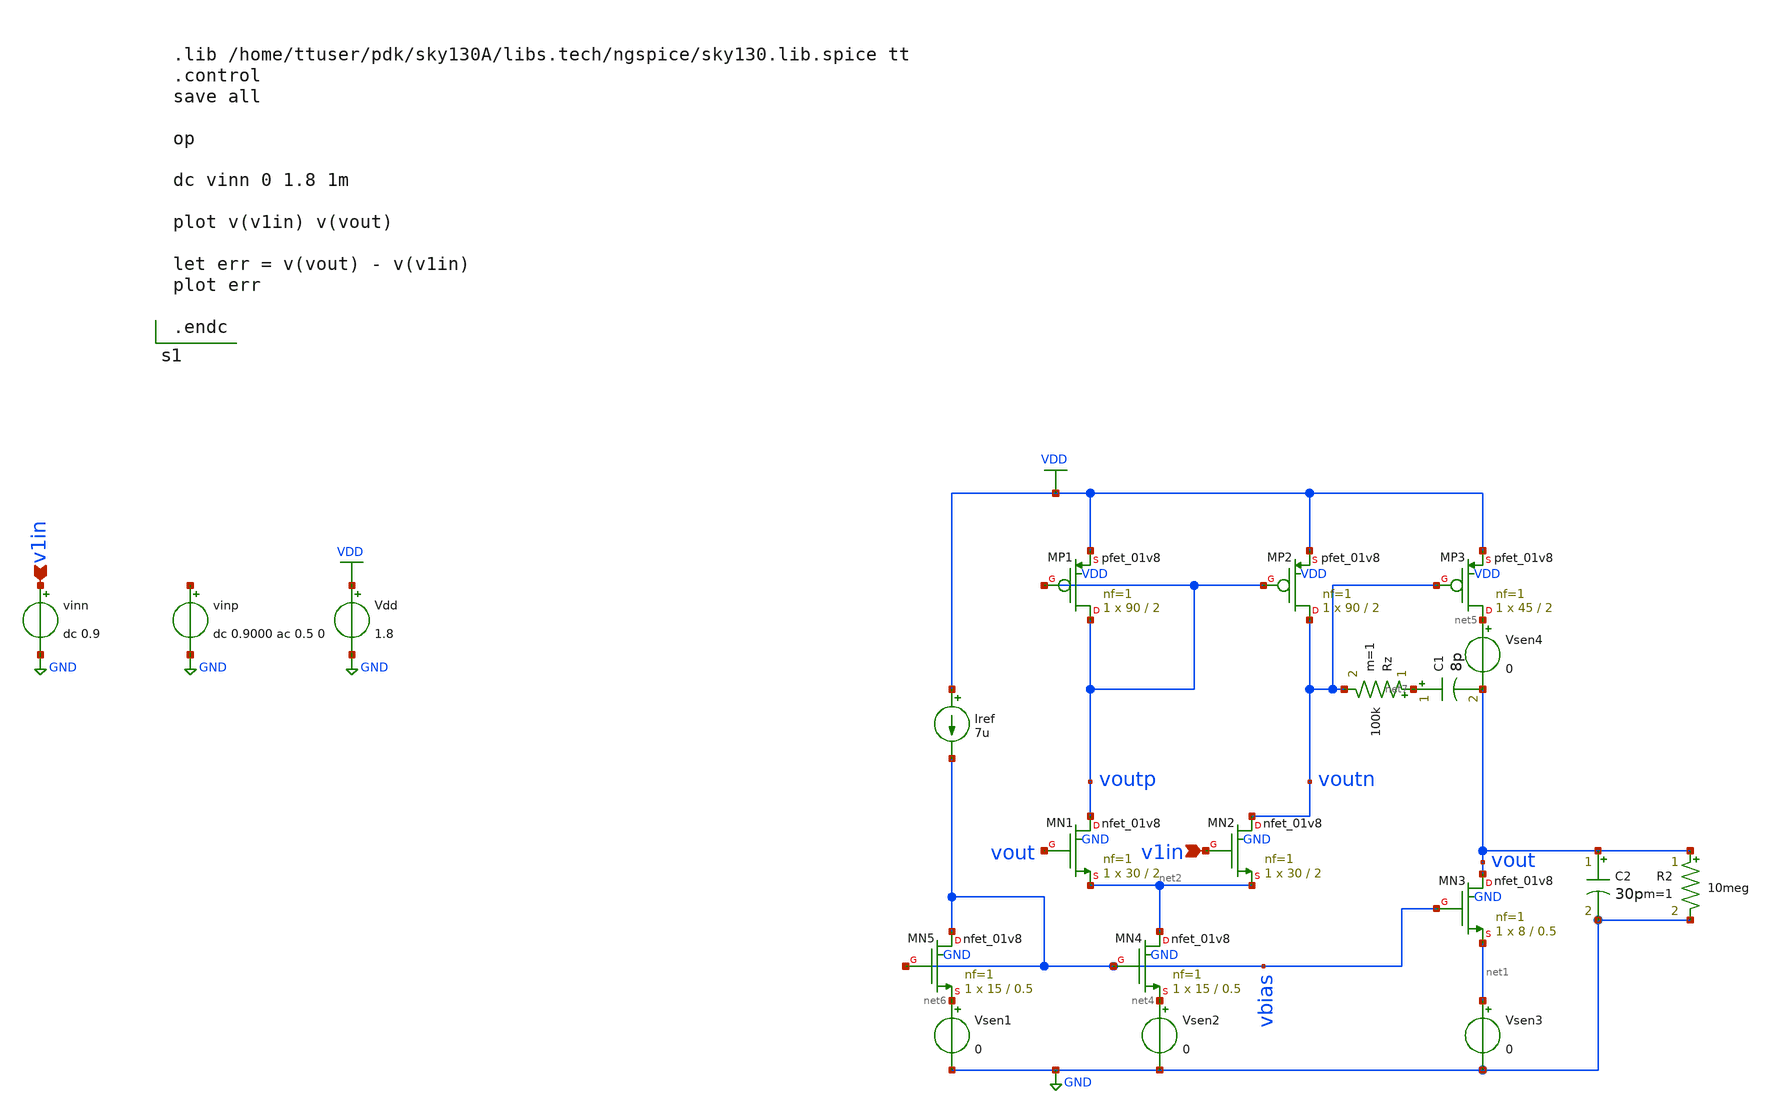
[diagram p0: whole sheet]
** sch_path: testbenches/prelayout/diffpairUnityFollower.sch
**.subckt diffpairUnityFollower v1in v1in
*.ipin v1in
*.ipin v1in
Vdd VDD GND 1.8
vinp net3 GND dc 0.9000 ac 0.5 0
vinn v1in GND dc 0.9
XMN1 voutp vout net2 GND sky130_fd_pr__nfet_01v8 L=2 W=30 nf=1 ad='int((nf+1)/2) * W/nf * 0.29' as='int((nf+2)/2) * W/nf * 0.29'
+ pd='2*int((nf+1)/2) * (W/nf + 0.29)' ps='2*int((nf+2)/2) * (W/nf + 0.29)' nrd='0.29 / W' nrs='0.29 / W'
+ sa=0 sb=0 sd=0 mult=1 m=1
XMN2 voutn v1in net2 GND sky130_fd_pr__nfet_01v8 L=2 W=30 nf=1 ad='int((nf+1)/2) * W/nf * 0.29' as='int((nf+2)/2) * W/nf * 0.29'
+ pd='2*int((nf+1)/2) * (W/nf + 0.29)' ps='2*int((nf+2)/2) * (W/nf + 0.29)' nrd='0.29 / W' nrs='0.29 / W'
+ sa=0 sb=0 sd=0 mult=1 m=1
XMP1 voutp voutp VDD VDD sky130_fd_pr__pfet_01v8 L=2 W=90 nf=1 ad='int((nf+1)/2) * W/nf * 0.29' as='int((nf+2)/2) * W/nf * 0.29'
+ pd='2*int((nf+1)/2) * (W/nf + 0.29)' ps='2*int((nf+2)/2) * (W/nf + 0.29)' nrd='0.29 / W' nrs='0.29 / W'
+ sa=0 sb=0 sd=0 mult=1 m=1
XMP2 voutn voutp VDD VDD sky130_fd_pr__pfet_01v8 L=2 W=90 nf=1 ad='int((nf+1)/2) * W/nf * 0.29' as='int((nf+2)/2) * W/nf * 0.29'
+ pd='2*int((nf+1)/2) * (W/nf + 0.29)' ps='2*int((nf+2)/2) * (W/nf + 0.29)' nrd='0.29 / W' nrs='0.29 / W'
+ sa=0 sb=0 sd=0 mult=1 m=1
Iref VDD vbias 7u
Vsen2 net4 GND 0
XMP3 net5 voutn VDD VDD sky130_fd_pr__pfet_01v8 L=2 W=45 nf=1 ad='int((nf+1)/2) * W/nf * 0.29' as='int((nf+2)/2) * W/nf * 0.29'
+ pd='2*int((nf+1)/2) * (W/nf + 0.29)' ps='2*int((nf+2)/2) * (W/nf + 0.29)' nrd='0.29 / W' nrs='0.29 / W'
+ sa=0 sb=0 sd=0 mult=1 m=1
XMN3 vout vbias net1 GND sky130_fd_pr__nfet_01v8 L=0.5 W=8 nf=1 ad='int((nf+1)/2) * W/nf * 0.29' as='int((nf+2)/2) * W/nf * 0.29'
+ pd='2*int((nf+1)/2) * (W/nf + 0.29)' ps='2*int((nf+2)/2) * (W/nf + 0.29)' nrd='0.29 / W' nrs='0.29 / W'
+ sa=0 sb=0 sd=0 mult=1 m=1
Vsen3 net1 GND 0
Vsen1 net6 GND 0
C1 net7 vout 8p m=1
XMN4 net2 vbias net4 GND sky130_fd_pr__nfet_01v8 L=0.5 W=15 nf=1 ad='int((nf+1)/2) * W/nf * 0.29' as='int((nf+2)/2) * W/nf * 0.29'
+ pd='2*int((nf+1)/2) * (W/nf + 0.29)' ps='2*int((nf+2)/2) * (W/nf + 0.29)' nrd='0.29 / W' nrs='0.29 / W'
+ sa=0 sb=0 sd=0 mult=1 m=1
XMN5 vbias vbias net6 GND sky130_fd_pr__nfet_01v8 L=0.5 W=15 nf=1 ad='int((nf+1)/2) * W/nf * 0.29' as='int((nf+2)/2) * W/nf * 0.29'
+ pd='2*int((nf+1)/2) * (W/nf + 0.29)' ps='2*int((nf+2)/2) * (W/nf + 0.29)' nrd='0.29 / W' nrs='0.29 / W'
+ sa=0 sb=0 sd=0 mult=1 m=1
C2 vout GND 30p m=1
Rz net7 voutn 100k m=1
Vsen4 net5 vout 0
R2 vout GND 10meg m=1
**** begin user architecture code


.lib /home/ttuser/pdk/sky130A/libs.tech/ngspice/sky130.lib.spice tt
.control
save all

op

dc vinn 0 1.8 1m

plot v(v1in) v(vout)

let err = v(vout) - v(v1in)
plot err

.endc


**** end user architecture code
**.ends
.GLOBAL VDD
.GLOBAL GND
.end
